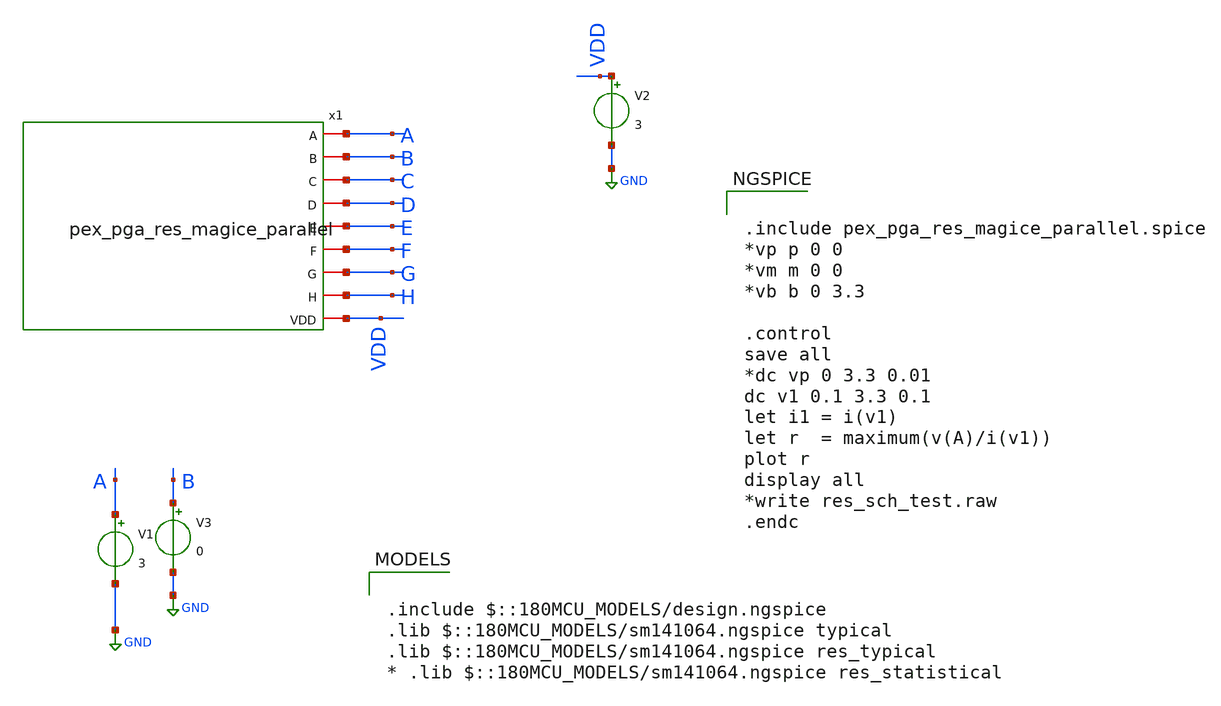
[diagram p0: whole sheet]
** sch_path: AWG_OUTPUT_AND_MUX_PAKISTAN_05/xschem/PEX_RES_TB.sch
**.subckt PEX_RES_TB
V1 A GND 3
V2 VDD GND 3
V3 B GND 0
x1 A B C D E F G H VDD pex_pga_res_magice_parallel
**** begin user architecture code

.include $::180MCU_MODELS/design.ngspice
.lib $::180MCU_MODELS/sm141064.ngspice typical
.lib $::180MCU_MODELS/sm141064.ngspice res_typical
* .lib $::180MCU_MODELS/sm141064.ngspice res_statistical



.include pex_pga_res_magice_parallel.spice
*vp p 0 0
*vm m 0 0
*vb b 0 3.3

.control
save all
*dc vp 0 3.3 0.01
dc v1 0.1 3.3 0.1
let i1 = i(v1)
let r  = maximum(v(A)/i(v1))
plot r
display all
*write res_sch_test.raw
.endc


**** end user architecture code
**.ends
.GLOBAL GND
.end
